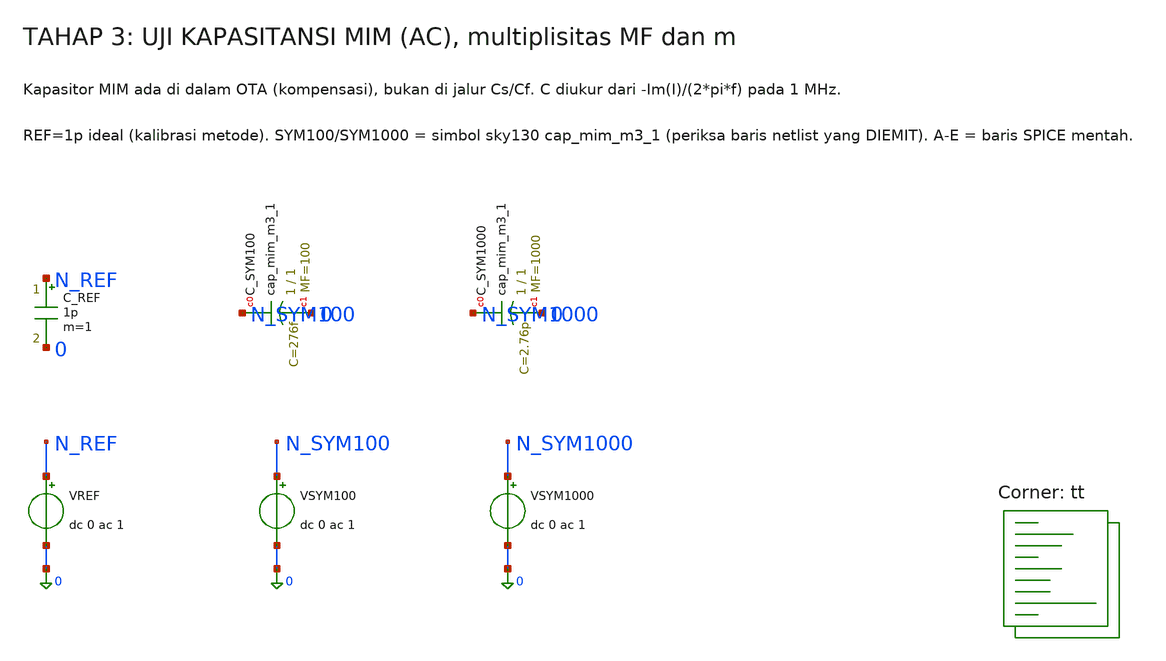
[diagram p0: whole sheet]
** sch_path: blocks/01_OTA/sim/tb_MIM_C_AC.sch
**.subckt tb_MIM_C_AC
VREF N_REF 0 dc 0 ac 1
VSYM100 N_SYM100 0 dc 0 ac 1
VSYM1000 N_SYM1000 0 dc 0 ac 1
C_REF N_REF 0 1p m=1
XC_SYM100 N_SYM100 0 sky130_fd_pr__cap_mim_m3_1 W=1 L=1 MF=100 m=100
XC_SYM1000 N_SYM1000 0 sky130_fd_pr__cap_mim_m3_1 W=1 L=1 MF=1000 m=1000
**** begin user architecture code
.lib $::SKYWATER_MODELS/sky130.lib.spice tt


* tahap 3: kapasitansi MIM via AC. TT, 27 C. Variabel dibedakan HANYA lewat MF dan m.
.option scale=1e-6
.temp 27
VA N_A 0 dc 0 ac 1
XCA N_A 0 sky130_fd_pr__cap_mim_m3_1 W=1 L=1 MF=100 m=100
VB N_B 0 dc 0 ac 1
XCB N_B 0 sky130_fd_pr__cap_mim_m3_1 W=1 L=1 MF=100 m=1
VC N_C 0 dc 0 ac 1
XCC N_C 0 sky130_fd_pr__cap_mim_m3_1 W=1 L=1 MF=1 m=100
VD N_D 0 dc 0 ac 1
XCD N_D 0 sky130_fd_pr__cap_mim_m3_1 W=1 L=1 MF=1000 m=1
VE N_E 0 dc 0 ac 1
XCE N_E 0 sky130_fd_pr__cap_mim_m3_1 W=1 L=1 MF=1 m=1
.control
set wr_singlescale
set wr_vecnames
set numdgt=12
ac dec 20 1e4 1e8
let w = 2*pi*real(frequency)
let C_REF = -imag(i(VREF))/w
let C_SYM100 = -imag(i(VSYM100))/w
let C_SYM1000 = -imag(i(VSYM1000))/w
let C_A = -imag(i(VA))/w
let C_B = -imag(i(VB))/w
let C_C = -imag(i(VC))/w
let C_D = -imag(i(VD))/w
let C_E = -imag(i(VE))/w
wrdata tb_MIM_C_AC.dat C_REF C_SYM100 C_SYM1000 C_A C_B C_C C_D C_E
echo TB_MIM_DONE
.endc


**** end user architecture code
**.ends
.end
